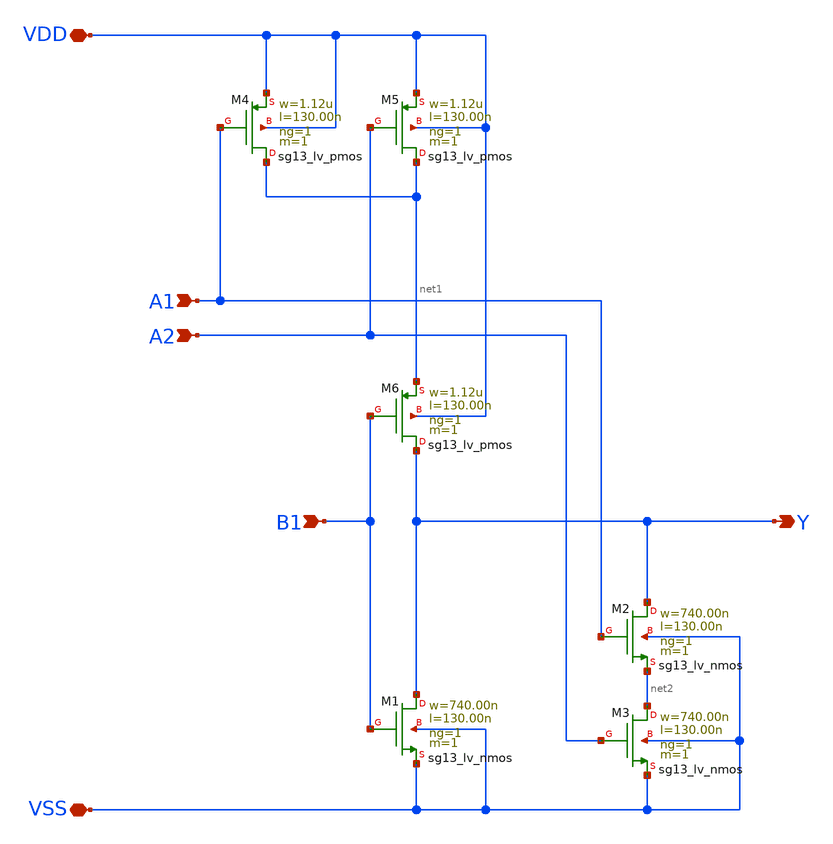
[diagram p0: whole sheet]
** sch_path: ihp-sg13g2/libs.tech/xschem/sg13g2_stdcells/sg13g2_a21oi_1.sch
**.subckt sg13g2_a21oi_1 A1 A2 B1 Y VDD VSS
*.ipin A1
*.ipin A2
*.ipin B1
*.opin Y
*.iopin VDD
*.iopin VSS
XM1 Y B1 VSS VSS sg13_lv_nmos w=740.00n l=130.00n ng=1 m=1 mm_ok=1
XM2 Y A1 net2 VSS sg13_lv_nmos w=740.00n l=130.00n ng=1 m=1 mm_ok=1
XM3 net2 A2 VSS VSS sg13_lv_nmos w=740.00n l=130.00n ng=1 m=1 mm_ok=1
XM4 net1 A1 VDD VDD sg13_lv_pmos w=1.12u l=130.00n ng=1 m=1 mm_ok=1
XM5 net1 A2 VDD VDD sg13_lv_pmos w=1.12u l=130.00n ng=1 m=1 mm_ok=1
XM6 Y B1 net1 VDD sg13_lv_pmos w=1.12u l=130.00n ng=1 m=1 mm_ok=1
**.ends
.end
